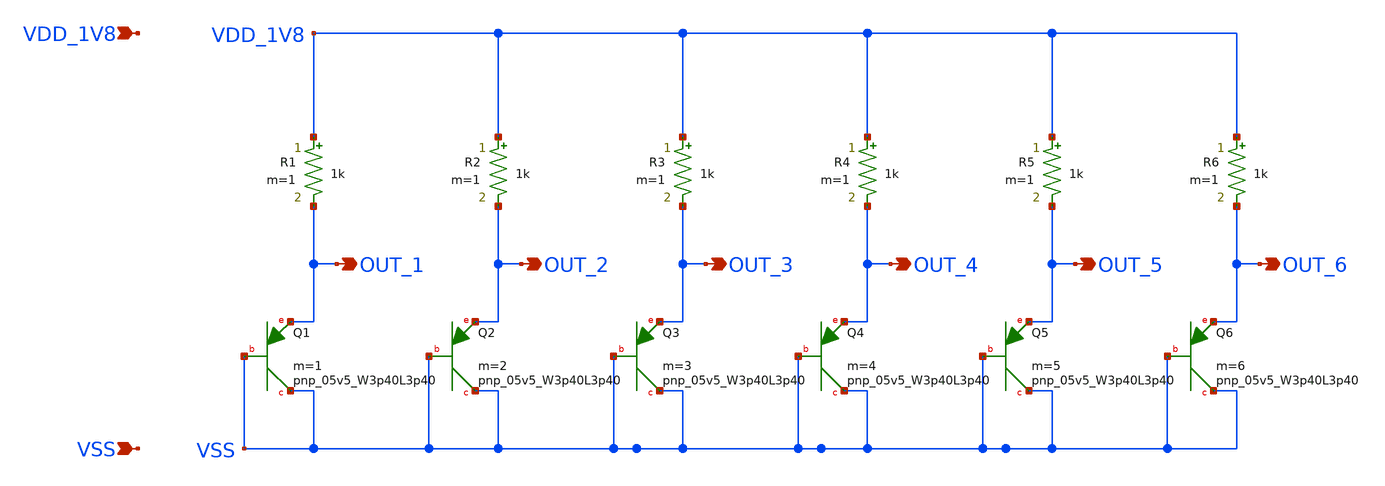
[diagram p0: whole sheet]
** sch_path: design/CNR_GR04_SKY130NM/DIFF_BJT.sch
**.subckt DIFF_BJT VDD_1V8 VSS OUT_1 OUT_2 OUT_3 OUT_4 OUT_5 OUT_6
*.ipin VDD_1V8
*.ipin VSS
*.opin OUT_1
*.opin OUT_2
*.opin OUT_3
*.opin OUT_4
*.opin OUT_5
*.opin OUT_6
XQ1 VSS VSS OUT_1 sky130_fd_pr__pnp_05v5_W3p40L3p40 m=1
XQ2 VSS VSS OUT_2 sky130_fd_pr__pnp_05v5_W3p40L3p40 m=2
R1 VDD_1V8 OUT_1 1k m=1
R2 VDD_1V8 OUT_2 1k m=1
R3 VDD_1V8 OUT_3 1k m=1
XQ3 VSS VSS OUT_3 sky130_fd_pr__pnp_05v5_W3p40L3p40 m=3
R4 VDD_1V8 OUT_4 1k m=1
XQ4 VSS VSS OUT_4 sky130_fd_pr__pnp_05v5_W3p40L3p40 m=4
R5 VDD_1V8 OUT_5 1k m=1
XQ5 VSS VSS OUT_5 sky130_fd_pr__pnp_05v5_W3p40L3p40 m=5
R6 VDD_1V8 OUT_6 1k m=1
XQ6 VSS VSS OUT_6 sky130_fd_pr__pnp_05v5_W3p40L3p40 m=6
**.ends
.end
